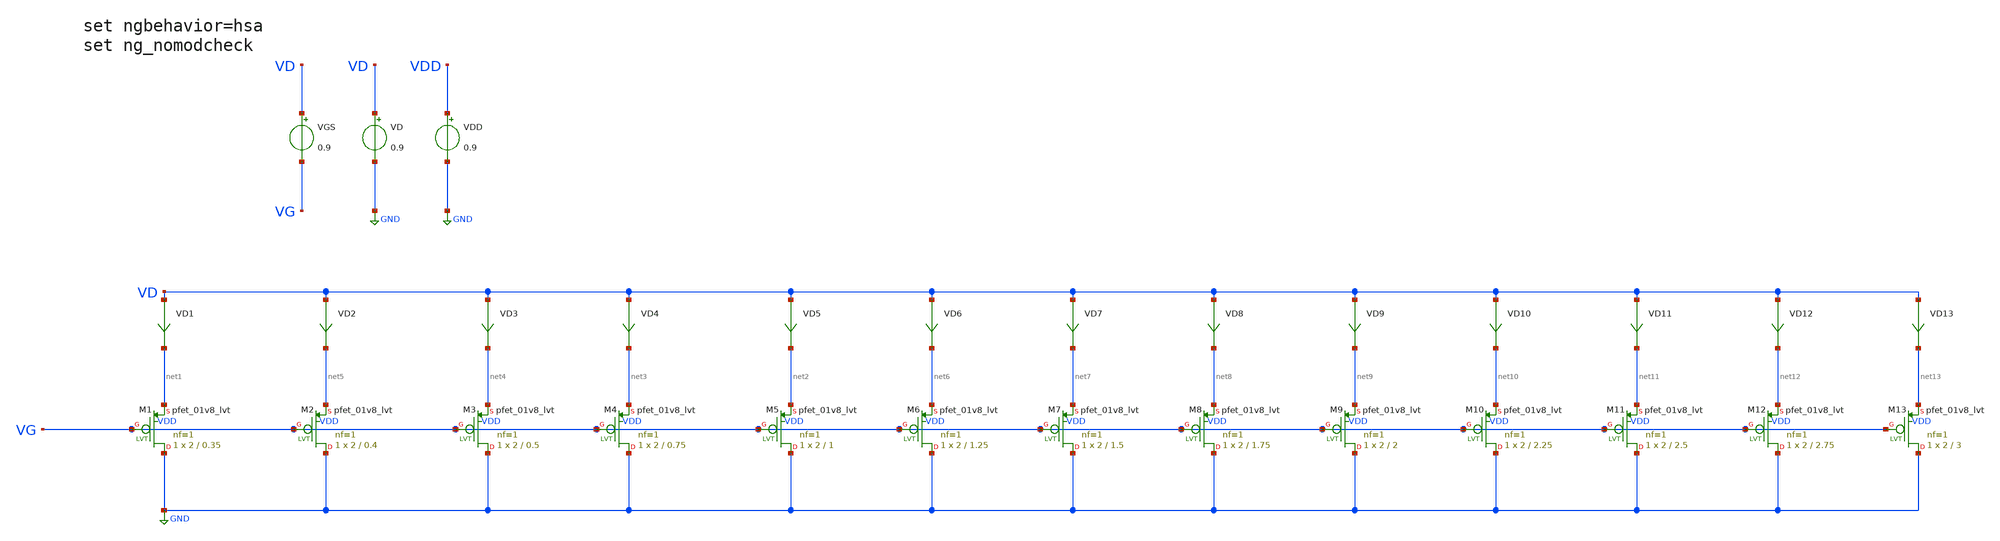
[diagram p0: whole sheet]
** sch_path: Designs/gmid_pmos_1v8_lvt_tb.sch
**.subckt gmid_pmos_1v8_lvt_tb
VGS VD VG 0.9
VD VD GND 0.9
VD1 VD net1 0
.save i(vd1)
VD2 VD net5 0
.save i(vd2)
VD3 VD net4 0
.save i(vd3)
VD4 VD net3 0
.save i(vd4)
VD5 VD net2 0
.save i(vd5)
VDD VDD GND 0.9
XM1 GND VG net1 VDD sky130_fd_pr__pfet_01v8_lvt L=0.35 W=2 nf=1 ad='int((nf+1)/2) * W/nf * 0.29' as='int((nf+2)/2) * W/nf * 0.29'
+ pd='2*int((nf+1)/2) * (W/nf + 0.29)' ps='2*int((nf+2)/2) * (W/nf + 0.29)' nrd='0.29 / W' nrs='0.29 / W'
+ sa=0 sb=0 sd=0 mult=1 m=1
XM2 GND VG net5 VDD sky130_fd_pr__pfet_01v8_lvt L=0.4 W=2 nf=1 ad='int((nf+1)/2) * W/nf * 0.29' as='int((nf+2)/2) * W/nf * 0.29'
+ pd='2*int((nf+1)/2) * (W/nf + 0.29)' ps='2*int((nf+2)/2) * (W/nf + 0.29)' nrd='0.29 / W' nrs='0.29 / W'
+ sa=0 sb=0 sd=0 mult=1 m=1
XM3 GND VG net4 VDD sky130_fd_pr__pfet_01v8_lvt L=0.5 W=2 nf=1 ad='int((nf+1)/2) * W/nf * 0.29' as='int((nf+2)/2) * W/nf * 0.29'
+ pd='2*int((nf+1)/2) * (W/nf + 0.29)' ps='2*int((nf+2)/2) * (W/nf + 0.29)' nrd='0.29 / W' nrs='0.29 / W'
+ sa=0 sb=0 sd=0 mult=1 m=1
XM4 GND VG net3 VDD sky130_fd_pr__pfet_01v8_lvt L=0.75 W=2 nf=1 ad='int((nf+1)/2) * W/nf * 0.29' as='int((nf+2)/2) * W/nf * 0.29'
+ pd='2*int((nf+1)/2) * (W/nf + 0.29)' ps='2*int((nf+2)/2) * (W/nf + 0.29)' nrd='0.29 / W' nrs='0.29 / W'
+ sa=0 sb=0 sd=0 mult=1 m=1
XM5 GND VG net2 VDD sky130_fd_pr__pfet_01v8_lvt L=1 W=2 nf=1 ad='int((nf+1)/2) * W/nf * 0.29' as='int((nf+2)/2) * W/nf * 0.29'
+ pd='2*int((nf+1)/2) * (W/nf + 0.29)' ps='2*int((nf+2)/2) * (W/nf + 0.29)' nrd='0.29 / W' nrs='0.29 / W'
+ sa=0 sb=0 sd=0 mult=1 m=1
XM6 GND VG net6 VDD sky130_fd_pr__pfet_01v8_lvt L=1.25 W=2 nf=1 ad='int((nf+1)/2) * W/nf * 0.29' as='int((nf+2)/2) * W/nf * 0.29'
+ pd='2*int((nf+1)/2) * (W/nf + 0.29)' ps='2*int((nf+2)/2) * (W/nf + 0.29)' nrd='0.29 / W' nrs='0.29 / W'
+ sa=0 sb=0 sd=0 mult=1 m=1
XM7 GND VG net7 VDD sky130_fd_pr__pfet_01v8_lvt L=1.5 W=2 nf=1 ad='int((nf+1)/2) * W/nf * 0.29' as='int((nf+2)/2) * W/nf * 0.29'
+ pd='2*int((nf+1)/2) * (W/nf + 0.29)' ps='2*int((nf+2)/2) * (W/nf + 0.29)' nrd='0.29 / W' nrs='0.29 / W'
+ sa=0 sb=0 sd=0 mult=1 m=1
XM8 GND VG net8 VDD sky130_fd_pr__pfet_01v8_lvt L=1.75 W=2 nf=1 ad='int((nf+1)/2) * W/nf * 0.29' as='int((nf+2)/2) * W/nf * 0.29'
+ pd='2*int((nf+1)/2) * (W/nf + 0.29)' ps='2*int((nf+2)/2) * (W/nf + 0.29)' nrd='0.29 / W' nrs='0.29 / W'
+ sa=0 sb=0 sd=0 mult=1 m=1
XM9 GND VG net9 VDD sky130_fd_pr__pfet_01v8_lvt L=2 W=2 nf=1 ad='int((nf+1)/2) * W/nf * 0.29' as='int((nf+2)/2) * W/nf * 0.29'
+ pd='2*int((nf+1)/2) * (W/nf + 0.29)' ps='2*int((nf+2)/2) * (W/nf + 0.29)' nrd='0.29 / W' nrs='0.29 / W'
+ sa=0 sb=0 sd=0 mult=1 m=1
XM10 GND VG net10 VDD sky130_fd_pr__pfet_01v8_lvt L=2.25 W=2 nf=1 ad='int((nf+1)/2) * W/nf * 0.29' as='int((nf+2)/2) * W/nf * 0.29'
+ pd='2*int((nf+1)/2) * (W/nf + 0.29)' ps='2*int((nf+2)/2) * (W/nf + 0.29)' nrd='0.29 / W' nrs='0.29 / W'
+ sa=0 sb=0 sd=0 mult=1 m=1
XM11 GND VG net11 VDD sky130_fd_pr__pfet_01v8_lvt L=2.5 W=2 nf=1 ad='int((nf+1)/2) * W/nf * 0.29' as='int((nf+2)/2) * W/nf * 0.29'
+ pd='2*int((nf+1)/2) * (W/nf + 0.29)' ps='2*int((nf+2)/2) * (W/nf + 0.29)' nrd='0.29 / W' nrs='0.29 / W'
+ sa=0 sb=0 sd=0 mult=1 m=1
XM12 GND VG net12 VDD sky130_fd_pr__pfet_01v8_lvt L=2.75 W=2 nf=1 ad='int((nf+1)/2) * W/nf * 0.29' as='int((nf+2)/2) * W/nf * 0.29'
+ pd='2*int((nf+1)/2) * (W/nf + 0.29)' ps='2*int((nf+2)/2) * (W/nf + 0.29)' nrd='0.29 / W' nrs='0.29 / W'
+ sa=0 sb=0 sd=0 mult=1 m=1
XM13 GND VG net13 VDD sky130_fd_pr__pfet_01v8_lvt L=3 W=2 nf=1 ad='int((nf+1)/2) * W/nf * 0.29' as='int((nf+2)/2) * W/nf * 0.29'
+ pd='2*int((nf+1)/2) * (W/nf + 0.29)' ps='2*int((nf+2)/2) * (W/nf + 0.29)' nrd='0.29 / W' nrs='0.29 / W'
+ sa=0 sb=0 sd=0 mult=1 m=1
VD6 VD net6 0
.save i(vd6)
VD7 VD net7 0
.save i(vd7)
VD8 VD net8 0
.save i(vd8)
VD9 VD net9 0
.save i(vd9)
VD10 VD net10 0
.save i(vd10)
VD11 VD net11 0
.save i(vd11)
VD12 VD net12 0
.save i(vd12)
VD13 VD net13 0
.save i(vd13)
**** begin user architecture code

** opencircuitdesign pdks install
.lib $::SKYWATER_MODELS/sky130.lib.spice ff




* ngspice commands
.option wnflag=1
.option savecurrents
.control
save all
save @m.xm1.msky130_fd_pr__pfet_01v8_lvt[gm]
save @m.xm2.msky130_fd_pr__pfet_01v8_lvt[gm]
save @m.xm3.msky130_fd_pr__pfet_01v8_lvt[gm]
save @m.xm4.msky130_fd_pr__pfet_01v8_lvt[gm]
save @m.xm5.msky130_fd_pr__pfet_01v8_lvt[gm]
save @m.xm6.msky130_fd_pr__pfet_01v8_lvt[gm]
save @m.xm7.msky130_fd_pr__pfet_01v8_lvt[gm]
save @m.xm8.msky130_fd_pr__pfet_01v8_lvt[gm]
save @m.xm9.msky130_fd_pr__pfet_01v8_lvt[gm]
save @m.xm10.msky130_fd_pr__pfet_01v8_lvt[gm]
save @m.xm11.msky130_fd_pr__pfet_01v8_lvt[gm]
save @m.xm12.msky130_fd_pr__pfet_01v8_lvt[gm]
save @m.xm13.msky130_fd_pr__pfet_01v8_lvt[gm]
save @m.xm1.msky130_fd_pr__pfet_01v8_lvt[id]
save @m.xm2.msky130_fd_pr__pfet_01v8_lvt[id]
save @m.xm3.msky130_fd_pr__pfet_01v8_lvt[id]
save @m.xm4.msky130_fd_pr__pfet_01v8_lvt[id]
save @m.xm5.msky130_fd_pr__pfet_01v8_lvt[id]
save @m.xm6.msky130_fd_pr__pfet_01v8_lvt[id]
save @m.xm7.msky130_fd_pr__pfet_01v8_lvt[id]
save @m.xm8.msky130_fd_pr__pfet_01v8_lvt[id]
save @m.xm9.msky130_fd_pr__pfet_01v8_lvt[id]
save @m.xm10.msky130_fd_pr__pfet_01v8_lvt[id]
save @m.xm11.msky130_fd_pr__pfet_01v8_lvt[id]
save @m.xm12.msky130_fd_pr__pfet_01v8_lvt[id]
save @m.xm13.msky130_fd_pr__pfet_01v8_lvt[id]
save @m.xm1.msky130_fd_pr__pfet_01v8_lvt[vth]
save @m.xm2.msky130_fd_pr__pfet_01v8_lvt[vth]
save @m.xm3.msky130_fd_pr__pfet_01v8_lvt[vth]
save @m.xm4.msky130_fd_pr__pfet_01v8_lvt[vth]
save @m.xm5.msky130_fd_pr__pfet_01v8_lvt[vth]
save @m.xm6.msky130_fd_pr__pfet_01v8_lvt[vth]
save @m.xm7.msky130_fd_pr__pfet_01v8_lvt[vth]
save @m.xm8.msky130_fd_pr__pfet_01v8_lvt[vth]
save @m.xm9.msky130_fd_pr__pfet_01v8_lvt[vth]
save @m.xm10.msky130_fd_pr__pfet_01v8_lvt[vth]
save @m.xm11.msky130_fd_pr__pfet_01v8_lvt[vth]
save @m.xm12.msky130_fd_pr__pfet_01v8_lvt[vth]
save @m.xm13.msky130_fd_pr__pfet_01v8_lvt[vth]
save @m.xm1.msky130_fd_pr__pfet_01v8_lvt[gds]
save @m.xm2.msky130_fd_pr__pfet_01v8_lvt[gds]
save @m.xm3.msky130_fd_pr__pfet_01v8_lvt[gds]
save @m.xm4.msky130_fd_pr__pfet_01v8_lvt[gds]
save @m.xm5.msky130_fd_pr__pfet_01v8_lvt[gds]
save @m.xm6.msky130_fd_pr__pfet_01v8_lvt[gds]
save @m.xm7.msky130_fd_pr__pfet_01v8_lvt[gds]
save @m.xm8.msky130_fd_pr__pfet_01v8_lvt[gds]
save @m.xm9.msky130_fd_pr__pfet_01v8_lvt[gds]
save @m.xm10.msky130_fd_pr__pfet_01v8_lvt[gds]
save @m.xm11.msky130_fd_pr__pfet_01v8_lvt[gds]
save @m.xm12.msky130_fd_pr__pfet_01v8_lvt[gds]
save @m.xm13.msky130_fd_pr__pfet_01v8_lvt[gds]
save @m.xm1.msky130_fd_pr__pfet_01v8_lvt[cgg]
save @m.xm2.msky130_fd_pr__pfet_01v8_lvt[cgg]
save @m.xm3.msky130_fd_pr__pfet_01v8_lvt[cgg]
save @m.xm4.msky130_fd_pr__pfet_01v8_lvt[cgg]
save @m.xm5.msky130_fd_pr__pfet_01v8_lvt[cgg]
save @m.xm6.msky130_fd_pr__pfet_01v8_lvt[cgg]
save @m.xm7.msky130_fd_pr__pfet_01v8_lvt[cgg]
save @m.xm8.msky130_fd_pr__pfet_01v8_lvt[cgg]
save @m.xm9.msky130_fd_pr__pfet_01v8_lvt[cgg]
save @m.xm10.msky130_fd_pr__pfet_01v8_lvt[cgg]
save @m.xm11.msky130_fd_pr__pfet_01v8_lvt[cgg]
save @m.xm12.msky130_fd_pr__pfet_01v8_lvt[cgg]
save @m.xm13.msky130_fd_pr__pfet_01v8_lvt[cgg]
save @m.xm1.msky130_fd_pr__pfet_01v8_lvt[cgs]
save @m.xm2.msky130_fd_pr__pfet_01v8_lvt[cgs]
save @m.xm3.msky130_fd_pr__pfet_01v8_lvt[cgs]
save @m.xm4.msky130_fd_pr__pfet_01v8_lvt[cgs]
save @m.xm5.msky130_fd_pr__pfet_01v8_lvt[cgs]
save @m.xm6.msky130_fd_pr__pfet_01v8_lvt[cgs]
save @m.xm7.msky130_fd_pr__pfet_01v8_lvt[cgs]
save @m.xm8.msky130_fd_pr__pfet_01v8_lvt[cgs]
save @m.xm9.msky130_fd_pr__pfet_01v8_lvt[cgs]
save @m.xm10.msky130_fd_pr__pfet_01v8_lvt[cgs]
save @m.xm11.msky130_fd_pr__pfet_01v8_lvt[cgs]
save @m.xm12.msky130_fd_pr__pfet_01v8_lvt[cgs]
save @m.xm13.msky130_fd_pr__pfet_01v8_lvt[cgs]
save @m.xm1.msky130_fd_pr__pfet_01v8_lvt[cgd]
save @m.xm2.msky130_fd_pr__pfet_01v8_lvt[cgd]
save @m.xm3.msky130_fd_pr__pfet_01v8_lvt[cgd]
save @m.xm4.msky130_fd_pr__pfet_01v8_lvt[cgd]
save @m.xm5.msky130_fd_pr__pfet_01v8_lvt[cgd]
save @m.xm6.msky130_fd_pr__pfet_01v8_lvt[cgd]
save @m.xm7.msky130_fd_pr__pfet_01v8_lvt[cgd]
save @m.xm8.msky130_fd_pr__pfet_01v8_lvt[cgd]
save @m.xm9.msky130_fd_pr__pfet_01v8_lvt[cgd]
save @m.xm10.msky130_fd_pr__pfet_01v8_lvt[cgd]
save @m.xm11.msky130_fd_pr__pfet_01v8_lvt[cgd]
save @m.xm12.msky130_fd_pr__pfet_01v8_lvt[cgd]
save @m.xm13.msky130_fd_pr__pfet_01v8_lvt[cgd]
dc VGS 0.05 1.8 0.05
** remove zero length vectors to prevent write errors
remzerovec
write /home/nithinpuru/Desktop/OSIC/xschem/SKY130-sim/gmid_pmos_tb.raw
plot @m.xm1.msky130_fd_pr__pfet_01v8_lvt[gm]
plot @m.xm2.msky130_fd_pr__pfet_01v8_lvt[gm]
plot @m.xm3.msky130_fd_pr__pfet_01v8_lvt[gm]
plot @m.xm4.msky130_fd_pr__pfet_01v8_lvt[gm]
plot @m.xm5.msky130_fd_pr__pfet_01v8_lvt[gm]
plot @m.xm6.msky130_fd_pr__pfet_01v8_lvt[gm]
plot @m.xm7.msky130_fd_pr__pfet_01v8_lvt[gm]
plot @m.xm8.msky130_fd_pr__pfet_01v8_lvt[gm]
plot @m.xm9.msky130_fd_pr__pfet_01v8_lvt[gm]
plot @m.xm10.msky130_fd_pr__pfet_01v8_lvt[gm]
plot @m.xm11.msky130_fd_pr__pfet_01v8_lvt[gm]
plot @m.xm12.msky130_fd_pr__pfet_01v8_lvt[gm]
plot @m.xm13.msky130_fd_pr__pfet_01v8_lvt[gm]
wrdata /home/nithinpuru/Desktop/OSIC/xschem/SKY130-sim/gmid_pmos_1_pfet_01v8_lvt_tb.txt
+ @m.xm1.msky130_fd_pr__pfet_01v8_lvt[gm] i(VD1) @m.xm1.msky130_fd_pr__pfet_01v8_lvt[vth] @m.xm1.msky130_fd_pr__pfet_01v8_lvt[gds]
+ @m.xm1.msky130_fd_pr__pfet_01v8_lvt[cgg] @m.xm1.msky130_fd_pr__pfet_01v8_lvt[cgs] @m.xm1.msky130_fd_pr__pfet_01v8_lvt[cgd]
wrdata /home/nithinpuru/Desktop/OSIC/xschem/SKY130-sim/gmid_pmos_2_pfet_01v8_lvt_tb.txt
+ @m.xm2.msky130_fd_pr__pfet_01v8_lvt[gm] i(VD2) @m.xm2.msky130_fd_pr__pfet_01v8_lvt[vth] @m.xm2.msky130_fd_pr__pfet_01v8_lvt[gds]
+ @m.xm2.msky130_fd_pr__pfet_01v8_lvt[cgg] @m.xm2.msky130_fd_pr__pfet_01v8_lvt[cgs] @m.xm2.msky130_fd_pr__pfet_01v8_lvt[cgd]
wrdata /home/nithinpuru/Desktop/OSIC/xschem/SKY130-sim/gmid_pmos_3_pfet_01v8_lvt_tb.txt
+ @m.xm3.msky130_fd_pr__pfet_01v8_lvt[gm] i(VD3) @m.xm3.msky130_fd_pr__pfet_01v8_lvt[vth] @m.xm3.msky130_fd_pr__pfet_01v8_lvt[gds]
+ @m.xm3.msky130_fd_pr__pfet_01v8_lvt[cgg] @m.xm3.msky130_fd_pr__pfet_01v8_lvt[cgs] @m.xm3.msky130_fd_pr__pfet_01v8_lvt[cgd]
wrdata /home/nithinpuru/Desktop/OSIC/xschem/SKY130-sim/gmid_pmos_4_pfet_01v8_lvt_tb.txt
+ @m.xm4.msky130_fd_pr__pfet_01v8_lvt[gm] i(VD4) @m.xm4.msky130_fd_pr__pfet_01v8_lvt[vth] @m.xm4.msky130_fd_pr__pfet_01v8_lvt[gds]
+ @m.xm4.msky130_fd_pr__pfet_01v8_lvt[cgg] @m.xm4.msky130_fd_pr__pfet_01v8_lvt[cgs] @m.xm4.msky130_fd_pr__pfet_01v8_lvt[cgd]
wrdata /home/nithinpuru/Desktop/OSIC/xschem/SKY130-sim/gmid_pmos_5_pfet_01v8_lvt_tb.txt
+ @m.xm5.msky130_fd_pr__pfet_01v8_lvt[gm] i(VD5) @m.xm5.msky130_fd_pr__pfet_01v8_lvt[vth] @m.xm5.msky130_fd_pr__pfet_01v8_lvt[gds]
+ @m.xm5.msky130_fd_pr__pfet_01v8_lvt[cgg] @m.xm5.msky130_fd_pr__pfet_01v8_lvt[cgs] @m.xm5.msky130_fd_pr__pfet_01v8_lvt[cgd]
wrdata /home/nithinpuru/Desktop/OSIC/xschem/SKY130-sim/gmid_pmos_6_pfet_01v8_lvt_tb.txt
+ @m.xm6.msky130_fd_pr__pfet_01v8_lvt[gm] i(VD6) @m.xm6.msky130_fd_pr__pfet_01v8_lvt[vth] @m.xm6.msky130_fd_pr__pfet_01v8_lvt[gds]
+ @m.xm6.msky130_fd_pr__pfet_01v8_lvt[cgg] @m.xm6.msky130_fd_pr__pfet_01v8_lvt[cgs] @m.xm6.msky130_fd_pr__pfet_01v8_lvt[cgd]
wrdata /home/nithinpuru/Desktop/OSIC/xschem/SKY130-sim/gmid_pmos_7_pfet_01v8_lvt_tb.txt
+ @m.xm7.msky130_fd_pr__pfet_01v8_lvt[gm] i(VD7) @m.xm7.msky130_fd_pr__pfet_01v8_lvt[vth] @m.xm7.msky130_fd_pr__pfet_01v8_lvt[gds]
+ @m.xm7.msky130_fd_pr__pfet_01v8_lvt[cgg] @m.xm7.msky130_fd_pr__pfet_01v8_lvt[cgs] @m.xm7.msky130_fd_pr__pfet_01v8_lvt[cgd]
wrdata /home/nithinpuru/Desktop/OSIC/xschem/SKY130-sim/gmid_pmos_8_pfet_01v8_lvt_tb.txt
+ @m.xm8.msky130_fd_pr__pfet_01v8_lvt[gm] i(VD8) @m.xm8.msky130_fd_pr__pfet_01v8_lvt[vth] @m.xm8.msky130_fd_pr__pfet_01v8_lvt[gds]
+ @m.xm8.msky130_fd_pr__pfet_01v8_lvt[cgg] @m.xm8.msky130_fd_pr__pfet_01v8_lvt[cgs] @m.xm8.msky130_fd_pr__pfet_01v8_lvt[cgd]
wrdata /home/nithinpuru/Desktop/OSIC/xschem/SKY130-sim/gmid_pmos_9_pfet_01v8_lvt_tb.txt
+ @m.xm9.msky130_fd_pr__pfet_01v8_lvt[gm] i(VD9) @m.xm9.msky130_fd_pr__pfet_01v8_lvt[vth] @m.xm9.msky130_fd_pr__pfet_01v8_lvt[gds]
+ @m.xm9.msky130_fd_pr__pfet_01v8_lvt[cgg] @m.xm9.msky130_fd_pr__pfet_01v8_lvt[cgs] @m.xm9.msky130_fd_pr__pfet_01v8_lvt[cgd]
wrdata /home/nithinpuru/Desktop/OSIC/xschem/SKY130-sim/gmid_pmos_10_pfet_01v8_lvt_tb.txt
+ @m.xm10.msky130_fd_pr__pfet_01v8_lvt[gm] i(VD10) @m.xm10.msky130_fd_pr__pfet_01v8_lvt[vth] @m.xm10.msky130_fd_pr__pfet_01v8_lvt[gds]
+ @m.xm10.msky130_fd_pr__pfet_01v8_lvt[cgg] @m.xm10.msky130_fd_pr__pfet_01v8_lvt[cgs] @m.xm10.msky130_fd_pr__pfet_01v8_lvt[cgd]
wrdata /home/nithinpuru/Desktop/OSIC/xschem/SKY130-sim/gmid_pmos_11_pfet_01v8_lvt_tb.txt
+ @m.xm11.msky130_fd_pr__pfet_01v8_lvt[gm] i(VD11) @m.xm11.msky130_fd_pr__pfet_01v8_lvt[vth] @m.xm11.msky130_fd_pr__pfet_01v8_lvt[gds]
+ @m.xm11.msky130_fd_pr__pfet_01v8_lvt[cgg] @m.xm11.msky130_fd_pr__pfet_01v8_lvt[cgs] @m.xm11.msky130_fd_pr__pfet_01v8_lvt[cgd]
wrdata /home/nithinpuru/Desktop/OSIC/xschem/SKY130-sim/gmid_pmos_12_pfet_01v8_lvt_tb.txt
+ @m.xm12.msky130_fd_pr__pfet_01v8_lvt[gm] i(VD12) @m.xm12.msky130_fd_pr__pfet_01v8_lvt[vth] @m.xm12.msky130_fd_pr__pfet_01v8_lvt[gds]
+ @m.xm12.msky130_fd_pr__pfet_01v8_lvt[cgg] @m.xm12.msky130_fd_pr__pfet_01v8_lvt[cgs] @m.xm12.msky130_fd_pr__pfet_01v8_lvt[cgd]
wrdata /home/nithinpuru/Desktop/OSIC/xschem/SKY130-sim/gmid_pmos_13_pfet_01v8_lvt_tb.txt
+ @m.xm13.msky130_fd_pr__pfet_01v8_lvt[gm] i(VD13) @m.xm13.msky130_fd_pr__pfet_01v8_lvt[vth] @m.xm13.msky130_fd_pr__pfet_01v8_lvt[gds]
+ @m.xm13.msky130_fd_pr__pfet_01v8_lvt[cgg] @m.xm13.msky130_fd_pr__pfet_01v8_lvt[cgs] @m.xm13.msky130_fd_pr__pfet_01v8_lvt[cgd]

set appendwrite
op
remzerovec
write /home/nithinpuru/Desktop/OSIC/xschem/SKY130-sim/gmid_pmos_tb.raw
quit 0
.endc


**** end user architecture code
**.ends
.GLOBAL GND
.end
